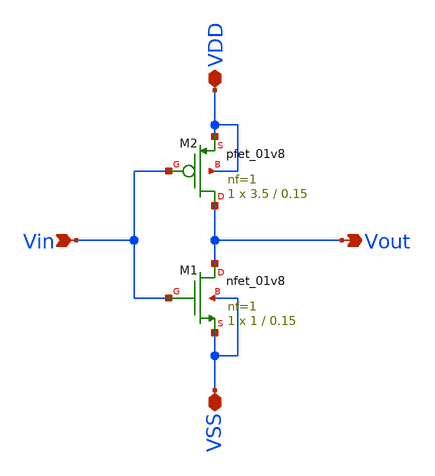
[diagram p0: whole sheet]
** sch_path: OneDrive/Documents/CMOS-Inverter-Design-and-Analysis-using-Sky130pdk-main/xschem/cmos_inv.sch
**.subckt cmos_inv VDD VSS Vin Vout
*.iopin VDD
*.iopin VSS
*.ipin Vin
*.opin Vout
XM1 Vout Vin VSS VSS sky130_fd_pr__nfet_01v8 L=0.15 W=1 nf=1 ad='int((1 + 1)/2) * 1 / 1 * 0.29' as='int((1 + 2)/2) * 1 / 1 * 0.29'
+ pd='2*int((1 + 1)/2) * (1 / 1 + 0.29)' ps='2*int((1 + 2)/2) * (1 / 1 + 0.29)' nrd='0.29 / 1 ' nrs='0.29 / 1 '
+ sa=0 sb=0 sd=0 mult=1 m=1
XM2 Vout Vin VDD VDD sky130_fd_pr__pfet_01v8 L=0.15 W=3.5 nf=1 ad='int((1 + 1)/2) * 3.5 / 1 * 0.29' as='int((1 + 2)/2) * 3.5 / 1 * 0.29'
+ pd='2*int((1 + 1)/2) * (3.5 / 1 + 0.29)' ps='2*int((1 + 2)/2) * (3.5 / 1 + 0.29)' nrd='0.29 / 3.5 ' nrs='0.29 / 3.5 '
+ sa=0 sb=0 sd=0 mult=1 m=1
**.ends
.end
